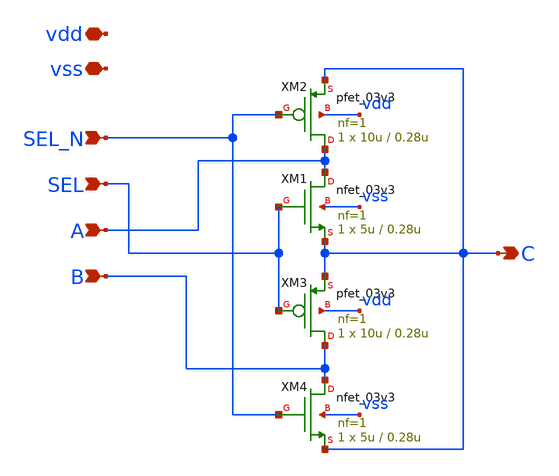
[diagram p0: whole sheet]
** sch_path: General/ADC/switching/mux_2to1_wo_single_select.sch
**.subckt mux_2to1_wo_single_select A B SEL C SEL_N vdd vss
*.ipin A
*.ipin B
*.ipin SEL
*.opin C
*.ipin SEL_N
*.iopin vdd
*.iopin vss
XM1 A SEL C vss nfet_03v3 L=0.28u W=5u nf=1 ad='int((nf+1)/2) * W/nf * 0.18u' as='int((nf+2)/2) * W/nf * 0.18u'
+ pd='2*int((nf+1)/2) * (W/nf + 0.18u)' ps='2*int((nf+2)/2) * (W/nf + 0.18u)' nrd='0.18u / W' nrs='0.18u / W'
+ sa=0 sb=0 sd=0 m=1
XM2 A SEL_N C vdd pfet_03v3 L=0.28u W=10u nf=1 ad='int((nf+1)/2) * W/nf * 0.18u' as='int((nf+2)/2) * W/nf * 0.18u'
+ pd='2*int((nf+1)/2) * (W/nf + 0.18u)' ps='2*int((nf+2)/2) * (W/nf + 0.18u)' nrd='0.18u / W' nrs='0.18u / W'
+ sa=0 sb=0 sd=0 m=1
XM3 B SEL C vdd pfet_03v3 L=0.28u W=10u nf=1 ad='int((nf+1)/2) * W/nf * 0.18u' as='int((nf+2)/2) * W/nf * 0.18u'
+ pd='2*int((nf+1)/2) * (W/nf + 0.18u)' ps='2*int((nf+2)/2) * (W/nf + 0.18u)' nrd='0.18u / W' nrs='0.18u / W'
+ sa=0 sb=0 sd=0 m=1
XM4 B SEL_N C vss nfet_03v3 L=0.28u W=5u nf=1 ad='int((nf+1)/2) * W/nf * 0.18u' as='int((nf+2)/2) * W/nf * 0.18u'
+ pd='2*int((nf+1)/2) * (W/nf + 0.18u)' ps='2*int((nf+2)/2) * (W/nf + 0.18u)' nrd='0.18u / W' nrs='0.18u / W'
+ sa=0 sb=0 sd=0 m=1
**.ends
.end
